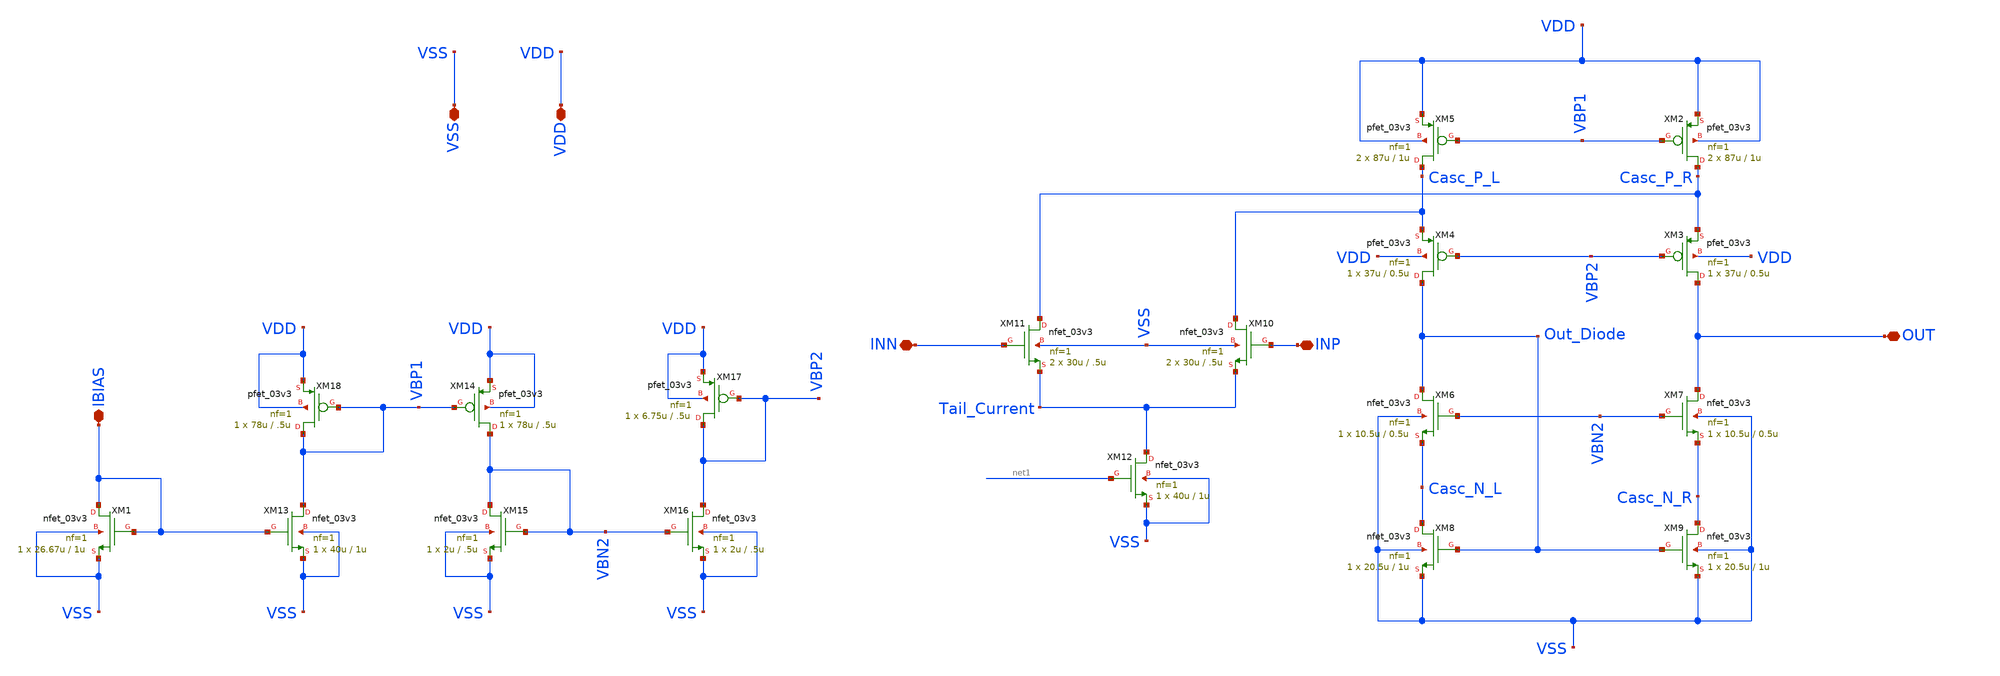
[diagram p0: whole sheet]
** sch_path: designs/libs/core_amps/ota_folded_cascode/etj_folded_new.sch
**.subckt etj_folded_new IBIAS VSS VDD INN INP OUT
*.iopin IBIAS
*.iopin VSS
*.iopin VDD
*.iopin INN
*.iopin INP
*.iopin OUT
XM1 IBIAS IBIAS VSS VSS nfet_03v3 L=1u W=26.67u nf=1 ad='int((nf+1)/2) * W/nf * 0.18u' as='int((nf+2)/2) * W/nf * 0.18u'
+ pd='2*int((nf+1)/2) * (W/nf + 0.18u)' ps='2*int((nf+2)/2) * (W/nf + 0.18u)' nrd='0.18u / W' nrs='0.18u / W'
+ sa=0 sb=0 sd=0 m=1
XM2 Casc_P_R VBP1 VDD VDD pfet_03v3 L=1u W=87u nf=1 ad='int((nf+1)/2) * W/nf * 0.18u' as='int((nf+2)/2) * W/nf * 0.18u'
+ pd='2*int((nf+1)/2) * (W/nf + 0.18u)' ps='2*int((nf+2)/2) * (W/nf + 0.18u)' nrd='0.18u / W' nrs='0.18u / W'
+ sa=0 sb=0 sd=0 m=2
XM3 OUT VBP2 Casc_P_R VDD pfet_03v3 L=0.5u W=37u nf=1 ad='int((nf+1)/2) * W/nf * 0.18u' as='int((nf+2)/2) * W/nf * 0.18u'
+ pd='2*int((nf+1)/2) * (W/nf + 0.18u)' ps='2*int((nf+2)/2) * (W/nf + 0.18u)' nrd='0.18u / W' nrs='0.18u / W'
+ sa=0 sb=0 sd=0 m=1
XM4 Out_Diode VBP2 Casc_P_L VDD pfet_03v3 L=0.5u W=37u nf=1 ad='int((nf+1)/2) * W/nf * 0.18u' as='int((nf+2)/2) * W/nf * 0.18u'
+ pd='2*int((nf+1)/2) * (W/nf + 0.18u)' ps='2*int((nf+2)/2) * (W/nf + 0.18u)' nrd='0.18u / W' nrs='0.18u / W'
+ sa=0 sb=0 sd=0 m=1
XM5 Casc_P_L VBP1 VDD VDD pfet_03v3 L=1u W=87u nf=1 ad='int((nf+1)/2) * W/nf * 0.18u' as='int((nf+2)/2) * W/nf * 0.18u'
+ pd='2*int((nf+1)/2) * (W/nf + 0.18u)' ps='2*int((nf+2)/2) * (W/nf + 0.18u)' nrd='0.18u / W' nrs='0.18u / W'
+ sa=0 sb=0 sd=0 m=2
XM6 Out_Diode VBN2 Casc_N_L VSS nfet_03v3 L=0.5u W=10.5u nf=1 ad='int((nf+1)/2) * W/nf * 0.18u' as='int((nf+2)/2) * W/nf * 0.18u'
+ pd='2*int((nf+1)/2) * (W/nf + 0.18u)' ps='2*int((nf+2)/2) * (W/nf + 0.18u)' nrd='0.18u / W' nrs='0.18u / W'
+ sa=0 sb=0 sd=0 m=1
XM7 OUT VBN2 Casc_N_R VSS nfet_03v3 L=0.5u W=10.5u nf=1 ad='int((nf+1)/2) * W/nf * 0.18u' as='int((nf+2)/2) * W/nf * 0.18u'
+ pd='2*int((nf+1)/2) * (W/nf + 0.18u)' ps='2*int((nf+2)/2) * (W/nf + 0.18u)' nrd='0.18u / W' nrs='0.18u / W'
+ sa=0 sb=0 sd=0 m=1
XM8 Casc_N_L Out_Diode VSS VSS nfet_03v3 L=1u W=20.5u nf=1 ad='int((nf+1)/2) * W/nf * 0.18u' as='int((nf+2)/2) * W/nf * 0.18u'
+ pd='2*int((nf+1)/2) * (W/nf + 0.18u)' ps='2*int((nf+2)/2) * (W/nf + 0.18u)' nrd='0.18u / W' nrs='0.18u / W'
+ sa=0 sb=0 sd=0 m=1
XM9 Casc_N_R Out_Diode VSS VSS nfet_03v3 L=1u W=20.5u nf=1 ad='int((nf+1)/2) * W/nf * 0.18u' as='int((nf+2)/2) * W/nf * 0.18u'
+ pd='2*int((nf+1)/2) * (W/nf + 0.18u)' ps='2*int((nf+2)/2) * (W/nf + 0.18u)' nrd='0.18u / W' nrs='0.18u / W'
+ sa=0 sb=0 sd=0 m=1
XM10 Casc_P_L INP Tail_Current VSS nfet_03v3 L=.5u W=30u nf=1 ad='int((nf+1)/2) * W/nf * 0.18u' as='int((nf+2)/2) * W/nf * 0.18u'
+ pd='2*int((nf+1)/2) * (W/nf + 0.18u)' ps='2*int((nf+2)/2) * (W/nf + 0.18u)' nrd='0.18u / W' nrs='0.18u / W'
+ sa=0 sb=0 sd=0 m=2
XM12 Tail_Current net1 VSS VSS nfet_03v3 L=1u W=40u nf=1 ad='int((nf+1)/2) * W/nf * 0.18u' as='int((nf+2)/2) * W/nf * 0.18u'
+ pd='2*int((nf+1)/2) * (W/nf + 0.18u)' ps='2*int((nf+2)/2) * (W/nf + 0.18u)' nrd='0.18u / W' nrs='0.18u / W'
+ sa=0 sb=0 sd=0 m=1
XM18 VBP1 VBP1 VDD VDD pfet_03v3 L=.5u W=78u nf=1 ad='int((nf+1)/2) * W/nf * 0.18u' as='int((nf+2)/2) * W/nf * 0.18u'
+ pd='2*int((nf+1)/2) * (W/nf + 0.18u)' ps='2*int((nf+2)/2) * (W/nf + 0.18u)' nrd='0.18u / W' nrs='0.18u / W'
+ sa=0 sb=0 sd=0 m=1
XM11 Casc_P_R INN Tail_Current VSS nfet_03v3 L=.5u W=30u nf=1 ad='int((nf+1)/2) * W/nf * 0.18u' as='int((nf+2)/2) * W/nf * 0.18u'
+ pd='2*int((nf+1)/2) * (W/nf + 0.18u)' ps='2*int((nf+2)/2) * (W/nf + 0.18u)' nrd='0.18u / W' nrs='0.18u / W'
+ sa=0 sb=0 sd=0 m=2
XM14 VBN2 VBP1 VDD VDD pfet_03v3 L=.5u W=78u nf=1 ad='int((nf+1)/2) * W/nf * 0.18u' as='int((nf+2)/2) * W/nf * 0.18u'
+ pd='2*int((nf+1)/2) * (W/nf + 0.18u)' ps='2*int((nf+2)/2) * (W/nf + 0.18u)' nrd='0.18u / W' nrs='0.18u / W'
+ sa=0 sb=0 sd=0 m=1
XM15 VBN2 VBN2 VSS VSS nfet_03v3 L=.5u W=2u nf=1 ad='int((nf+1)/2) * W/nf * 0.18u' as='int((nf+2)/2) * W/nf * 0.18u'
+ pd='2*int((nf+1)/2) * (W/nf + 0.18u)' ps='2*int((nf+2)/2) * (W/nf + 0.18u)' nrd='0.18u / W' nrs='0.18u / W'
+ sa=0 sb=0 sd=0 m=1
XM16 VBP2 VBN2 VSS VSS nfet_03v3 L=.5u W=2u nf=1 ad='int((nf+1)/2) * W/nf * 0.18u' as='int((nf+2)/2) * W/nf * 0.18u'
+ pd='2*int((nf+1)/2) * (W/nf + 0.18u)' ps='2*int((nf+2)/2) * (W/nf + 0.18u)' nrd='0.18u / W' nrs='0.18u / W'
+ sa=0 sb=0 sd=0 m=1
XM17 VBP2 VBP2 VDD VDD pfet_03v3 L=.5u W=6.75u nf=1 ad='int((nf+1)/2) * W/nf * 0.18u' as='int((nf+2)/2) * W/nf * 0.18u'
+ pd='2*int((nf+1)/2) * (W/nf + 0.18u)' ps='2*int((nf+2)/2) * (W/nf + 0.18u)' nrd='0.18u / W' nrs='0.18u / W'
+ sa=0 sb=0 sd=0 m=1
XM13 VBP1 IBIAS VSS VSS nfet_03v3 L=1u W=40u nf=1 ad='int((nf+1)/2) * W/nf * 0.18u' as='int((nf+2)/2) * W/nf * 0.18u'
+ pd='2*int((nf+1)/2) * (W/nf + 0.18u)' ps='2*int((nf+2)/2) * (W/nf + 0.18u)' nrd='0.18u / W' nrs='0.18u / W'
+ sa=0 sb=0 sd=0 m=1
**.ends
.end
